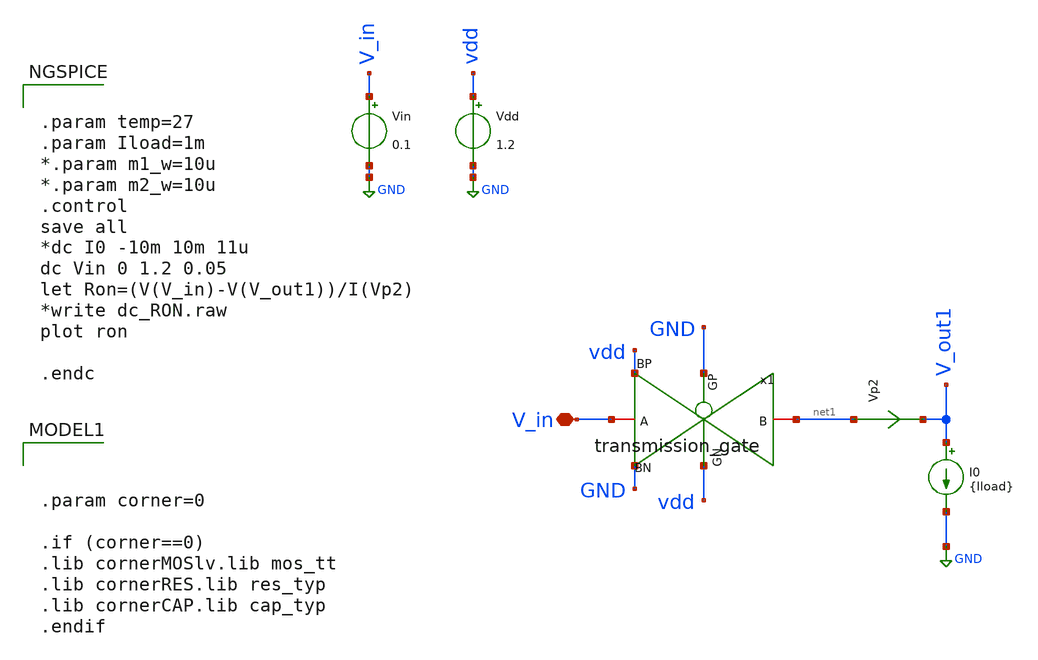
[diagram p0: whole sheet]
** sch_path: design_data/tb_tgate_RON.sch
**.subckt tb_tgate_RON V_in
*.iopin V_in
x1 net1 vdd GND V_in vdd GND transmission_gate
I0 V_out1 GND {Iload}
Vp2 net1 V_out1 0
.save i(vp2)
Vin V_in GND 0.1
Vdd vdd GND 1.2
**** begin user architecture code


.param temp=27
.param Iload=1m
*.param m1_w=10u
*.param m2_w=10u
.control
save all
*dc I0 -10m 10m 11u
dc Vin 0 1.2 0.05
let Ron=(V(V_in)-V(V_out1))/I(Vp2)
*write dc_RON.raw
plot ron

.endc




.param corner=0

.if (corner==0)
.lib cornerMOSlv.lib mos_tt
.lib cornerRES.lib res_typ
.lib cornerCAP.lib cap_typ
.endif

**** end user architecture code
**.ends

* expanding   symbol:  transmission_gate.sym # of pins=6
** sym_path: transmission_gate.sym
** sch_path: transmission_gate.sch
.subckt transmission_gate B GN GP A BP BN
*.iopin B
*.iopin GN
*.iopin A
*.iopin GP
*.iopin BN
*.iopin BP
XM1 A GN B BN sg13_lv_nmos w=10u l=0.13u ng=1 m=1 mm_ok=1
XM2 A GP B BP sg13_lv_pmos w=20u l=0.13u ng=2 m=1 mm_ok=1
.ends

.GLOBAL GND
.end
